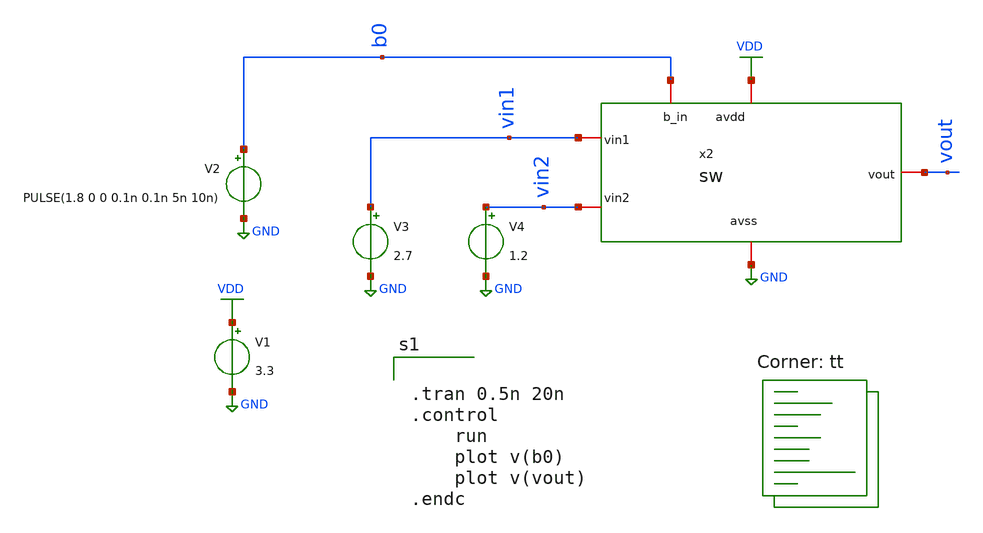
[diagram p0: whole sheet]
** sch_path: designs/libs/crossmem_ipn/dac4bits/sch/tb_switch.sch
**.subckt tb_switch
V1 VDD GND 3.3
V2 b0 GND PULSE(1.8 0 0 0.1n 0.1n 5n 10n)
V3 vin1 GND 2.7
V4 vin2 GND 1.2
x2 VDD b0 GND vin1 vout vin2 sw
**** begin user architecture code
.lib $::SKYWATER_MODELS/sky130.lib.spice tt


.tran 0.5n 20n
.control
	run
	plot v(b0)
	plot v(vout)
.endc



**** end user architecture code
**.ends

* expanding   symbol:  sw.sym # of pins=6
** sym_path: designs/libs/crossmem_ipn/dac4bits/sch/sw.sym
** sch_path: designs/libs/crossmem_ipn/dac4bits/sch/sw.sch
.subckt sw avdd b_in avss vin1 vout vin2
*.iopin avss
*.iopin vin1
*.iopin vout
*.iopin avdd
*.iopin vin2
*.iopin b_in
XM1 net1 b_in avss avss sky130_fd_pr__nfet_01v8 L=0.15 W=0.5 nf=1 ad='int((nf+1)/2) * W/nf * 0.29' as='int((nf+2)/2) * W/nf * 0.29'
+ pd='2*int((nf+1)/2) * (W/nf + 0.29)' ps='2*int((nf+2)/2) * (W/nf + 0.29)' nrd='0.29 / W' nrs='0.29 / W'
+ sa=0 sb=0 sd=0 mult=1 m=1
XM2 net1 b_in avdd avdd sky130_fd_pr__pfet_01v8 L=0.15 W=0.5 nf=1 ad='int((nf+1)/2) * W/nf * 0.29' as='int((nf+2)/2) * W/nf * 0.29'
+ pd='2*int((nf+1)/2) * (W/nf + 0.29)' ps='2*int((nf+2)/2) * (W/nf + 0.29)' nrd='0.29 / W' nrs='0.29 / W'
+ sa=0 sb=0 sd=0 mult=1 m=1
XM3 net2 net1 avss avss sky130_fd_pr__nfet_01v8 L=0.15 W=0.5 nf=1 ad='int((nf+1)/2) * W/nf * 0.29' as='int((nf+2)/2) * W/nf * 0.29'
+ pd='2*int((nf+1)/2) * (W/nf + 0.29)' ps='2*int((nf+2)/2) * (W/nf + 0.29)' nrd='0.29 / W' nrs='0.29 / W'
+ sa=0 sb=0 sd=0 mult=1 m=1
XM4 net2 net1 avdd avdd sky130_fd_pr__pfet_01v8 L=0.15 W=0.5 nf=1 ad='int((nf+1)/2) * W/nf * 0.29' as='int((nf+2)/2) * W/nf * 0.29'
+ pd='2*int((nf+1)/2) * (W/nf + 0.29)' ps='2*int((nf+2)/2) * (W/nf + 0.29)' nrd='0.29 / W' nrs='0.29 / W'
+ sa=0 sb=0 sd=0 mult=1 m=1
XM5 vout net1 vin1 avdd sky130_fd_pr__pfet_01v8 L=0.15 W=0.5 nf=1 ad='int((nf+1)/2) * W/nf * 0.29' as='int((nf+2)/2) * W/nf * 0.29'
+ pd='2*int((nf+1)/2) * (W/nf + 0.29)' ps='2*int((nf+2)/2) * (W/nf + 0.29)' nrd='0.29 / W' nrs='0.29 / W'
+ sa=0 sb=0 sd=0 mult=1 m=1
XM6 vout net1 vin2 avss sky130_fd_pr__nfet_01v8 L=0.15 W=0.5 nf=1 ad='int((nf+1)/2) * W/nf * 0.29' as='int((nf+2)/2) * W/nf * 0.29'
+ pd='2*int((nf+1)/2) * (W/nf + 0.29)' ps='2*int((nf+2)/2) * (W/nf + 0.29)' nrd='0.29 / W' nrs='0.29 / W'
+ sa=0 sb=0 sd=0 mult=1 m=1
XM7 vin1 net2 vout avss sky130_fd_pr__nfet_01v8 L=0.15 W=0.5 nf=1 ad='int((nf+1)/2) * W/nf * 0.29' as='int((nf+2)/2) * W/nf * 0.29'
+ pd='2*int((nf+1)/2) * (W/nf + 0.29)' ps='2*int((nf+2)/2) * (W/nf + 0.29)' nrd='0.29 / W' nrs='0.29 / W'
+ sa=0 sb=0 sd=0 mult=1 m=1
XM8 vin2 net2 vout avdd sky130_fd_pr__pfet_01v8 L=0.15 W=0.5 nf=1 ad='int((nf+1)/2) * W/nf * 0.29' as='int((nf+2)/2) * W/nf * 0.29'
+ pd='2*int((nf+1)/2) * (W/nf + 0.29)' ps='2*int((nf+2)/2) * (W/nf + 0.29)' nrd='0.29 / W' nrs='0.29 / W'
+ sa=0 sb=0 sd=0 mult=1 m=1
.ends

.GLOBAL VDD
.GLOBAL GND
.end
